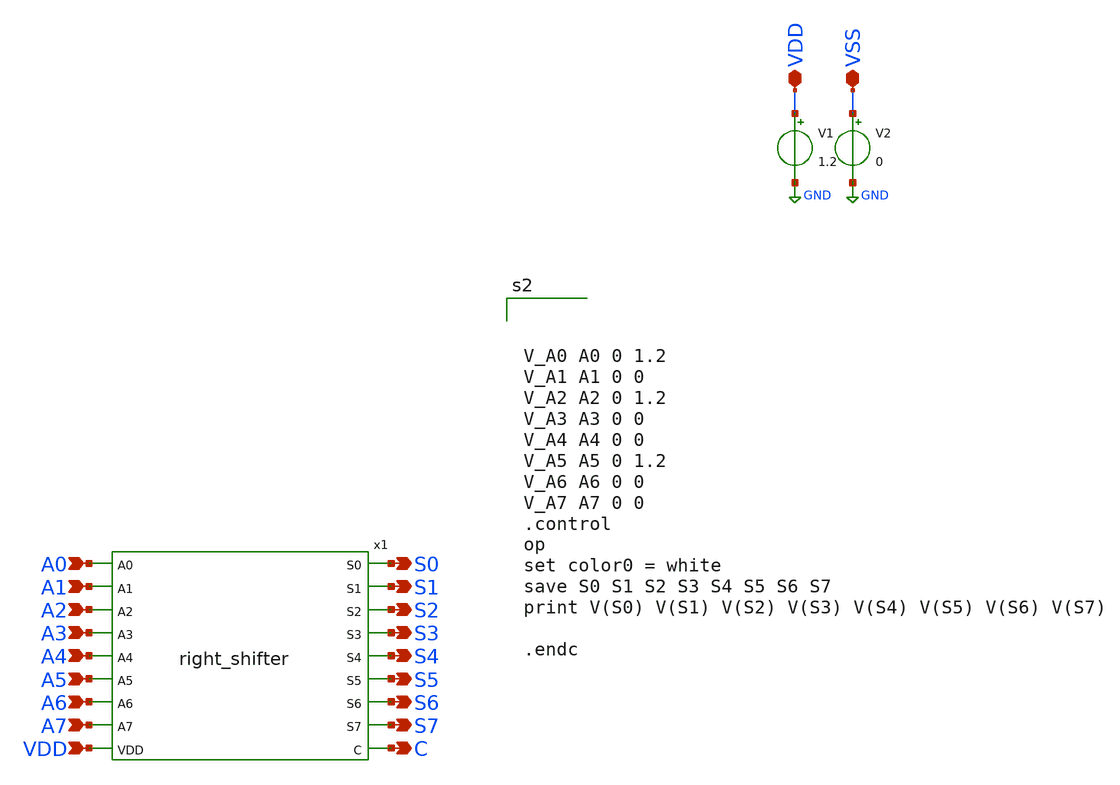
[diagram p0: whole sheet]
** sch_path: design/xschem/TEST_BENCHES/RIGHTSHIFTER_TB.sch
**.subckt RIGHTSHIFTER_TB A0 A1 A2 A3 A4 A5 A6 A7 S6 S7 S3 S4 S5 S0 S1 S2 C VDD VDD VSS
*.ipin A0
*.ipin A1
*.ipin A2
*.ipin A3
*.ipin A4
*.ipin A5
*.ipin A6
*.ipin A7
*.opin S6
*.opin S7
*.opin S3
*.opin S4
*.opin S5
*.opin S0
*.opin S1
*.opin S2
*.opin C
*.ipin VDD
*.iopin VDD
*.iopin VSS
x1 A0 A1 A2 A3 A4 A5 A6 A7 VDD S0 S1 S2 S3 S4 S5 S6 S7 C right_shifter
V1 VDD GND 1.2
V2 VSS GND 0
**** begin user architecture code



V_A0 A0 0 1.2
V_A1 A1 0 0
V_A2 A2 0 1.2
V_A3 A3 0 0
V_A4 A4 0 0
V_A5 A5 0 1.2
V_A6 A6 0 0
V_A7 A7 0 0
.control
op
set color0 = white
save S0 S1 S2 S3 S4 S5 S6 S7
print V(S0) V(S1) V(S2) V(S3) V(S4) V(S5) V(S6) V(S7)

.endc



** opencircuitdesign pdks install
.lib $::SKYWATER_MODELS/sky130.lib.spice tt_mm


**** end user architecture code
**.ends

* expanding   symbol:  SHIFTER/right_shifter.sym # of pins=18
** sym_path: design/xschem/SHIFTER/right_shifter.sym
** sch_path: design/xschem/SHIFTER/right_shifter.sch
.subckt right_shifter A0 A1 A2 A3 A4 A5 A6 A7 VDD S0 S1 S2 S3 S4 S5 S6 S7 C
*.ipin A7
*.opin S7
*.ipin A6
*.ipin A5
*.ipin A4
*.ipin A3
*.ipin A2
*.ipin A1
*.ipin A0
*.opin S6
*.opin S5
*.opin S4
*.opin S3
*.opin S2
*.opin S1
*.opin C
*.opin S0
*.ipin VDD
x1 A0 VSS VDD C buffer
x2 A1 VSS VDD S0 buffer
x3 A2 VSS VDD S1 buffer
x4 A3 VSS VDD S2 buffer
x5 A4 VSS VDD S3 buffer
x6 A5 VSS VDD S4 buffer
x7 A6 VSS VDD S5 buffer
x8 A7 VSS VDD S6 buffer
x9 VDD VSS VDD S7 inv
.ends


* expanding   symbol:  INV/buffer.sym # of pins=2
** sym_path: design/xschem/INV/buffer.sym
** sch_path: design/xschem/INV/buffer.sch
.subckt buffer A VSS VDD Y
*.ipin A
*.opin Y
x1 A VSS VDD net1 inv
x2 net1 VSS VDD Y inv
.ends


* expanding   symbol:  INV/inv.sym # of pins=2
** sym_path: design/xschem/INV/inv.sym
** sch_path: design/xschem/INV/inv.sch
.subckt inv A VSS VDD Y
*.ipin A
*.opin Y
XM2 Y A VSS GND sky130_fd_pr__nfet_01v8 L=0.15 W=1 nf=1 ad='int((nf+1)/2) * W/nf * 0.29' as='int((nf+2)/2) * W/nf * 0.29'
+ pd='2*int((nf+1)/2) * (W/nf + 0.29)' ps='2*int((nf+2)/2) * (W/nf + 0.29)' nrd='0.29 / W' nrs='0.29 / W'
+ sa=0 sb=0 sd=0 mult=1 m=1
XM1 Y A VDD VDD sky130_fd_pr__pfet_01v8 L=0.15 W=3.21 nf=1 ad='int((nf+1)/2) * W/nf * 0.29' as='int((nf+2)/2) * W/nf * 0.29'
+ pd='2*int((nf+1)/2) * (W/nf + 0.29)' ps='2*int((nf+2)/2) * (W/nf + 0.29)' nrd='0.29 / W' nrs='0.29 / W'
+ sa=0 sb=0 sd=0 mult=1 m=1
.ends

.GLOBAL GND
.end
